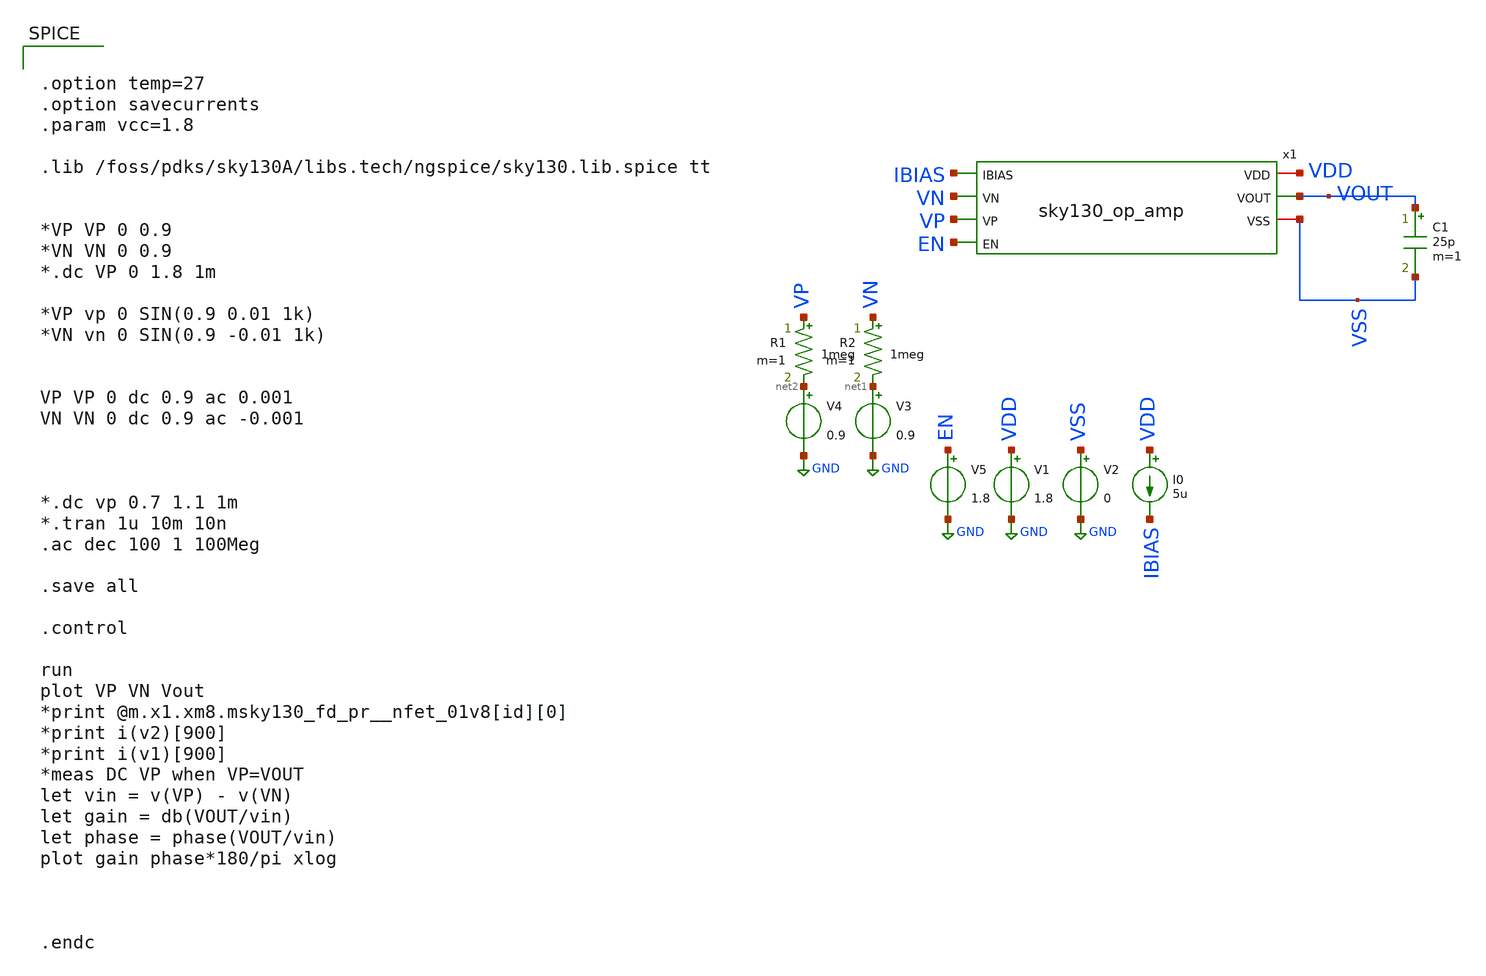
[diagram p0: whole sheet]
** sch_path: xschem/sky130_op_amp_tb.sch
**.subckt sky130_op_amp_tb
C1 VOUT VSS 25p m=1
V2 VSS GND 0
I0 VDD IBIAS 5u
V3 net1 GND 0.9
V4 net2 GND 0.9
V5 EN GND 1.8
R1 VP net2 1meg m=1
R2 VN net1 1meg m=1
V1 VDD GND 1.8
x1 VDD IBIAS VN VP VOUT EN VSS sky130_op_amp
**** begin user architecture code


.option temp=27
.option savecurrents
.param vcc=1.8

.lib /foss/pdks/sky130A/libs.tech/ngspice/sky130.lib.spice tt


*VP VP 0 0.9
*VN VN 0 0.9
*.dc VP 0 1.8 1m

*VP vp 0 SIN(0.9 0.01 1k)
*VN vn 0 SIN(0.9 -0.01 1k)


VP VP 0 dc 0.9 ac 0.001
VN VN 0 dc 0.9 ac -0.001



*.dc vp 0.7 1.1 1m
*.tran 1u 10m 10n
.ac dec 100 1 100Meg

.save all

.control

run
plot VP VN Vout
*print @m.x1.xm8.msky130_fd_pr__nfet_01v8[id][0]
*print i(v2)[900]
*print i(v1)[900]
*meas DC VP when VP=VOUT
let vin = v(VP) - v(VN)
let gain = db(VOUT/vin)
let phase = phase(VOUT/vin)
plot gain phase*180/pi xlog



.endc





**** end user architecture code
**.ends

* expanding   symbol:  sky130_op_amp.sym # of pins=7
** sym_path: xschem/sky130_op_amp.sym
** sch_path: xschem/sky130_op_amp.sch
.subckt sky130_op_amp VDD IBIAS VN VP VOUT EN VSS
*.ipin VN
*.opin VOUT
*.iopin VDD
*.iopin VSS
*.ipin VP
*.ipin EN
*.ipin IBIAS
XM1 D1 VN VTAIL VSS sky130_fd_pr__nfet_01v8 L=1 W=4 nf=4 ad='int((nf+1)/2) * W/nf * 0.29' as='int((nf+2)/2) * W/nf * 0.29'
+ pd='2*int((nf+1)/2) * (W/nf + 0.29)' ps='2*int((nf+2)/2) * (W/nf + 0.29)' nrd='0.29 / W' nrs='0.29 / W'
+ sa=0 sb=0 sd=0 mult=4 m=4
XM2 D2 VP VTAIL VSS sky130_fd_pr__nfet_01v8 L=1 W=4 nf=4 ad='int((nf+1)/2) * W/nf * 0.29' as='int((nf+2)/2) * W/nf * 0.29'
+ pd='2*int((nf+1)/2) * (W/nf + 0.29)' ps='2*int((nf+2)/2) * (W/nf + 0.29)' nrd='0.29 / W' nrs='0.29 / W'
+ sa=0 sb=0 sd=0 mult=4 m=4
XM5 VTAIL IBIAS m5m9_net VSS sky130_fd_pr__nfet_01v8 L=1 W=5 nf=4 ad='int((nf+1)/2) * W/nf * 0.29' as='int((nf+2)/2) * W/nf * 0.29'
+ pd='2*int((nf+1)/2) * (W/nf + 0.29)' ps='2*int((nf+2)/2) * (W/nf + 0.29)' nrd='0.29 / W' nrs='0.29 / W'
+ sa=0 sb=0 sd=0 mult=8 m=8
XM8 IBIAS IBIAS net1 VSS sky130_fd_pr__nfet_01v8 L=1 W=4 nf=4 ad='int((nf+1)/2) * W/nf * 0.29' as='int((nf+2)/2) * W/nf * 0.29'
+ pd='2*int((nf+1)/2) * (W/nf + 0.29)' ps='2*int((nf+2)/2) * (W/nf + 0.29)' nrd='0.29 / W' nrs='0.29 / W'
+ sa=0 sb=0 sd=0 mult=1 m=1
XM3 D1 D1 VDD VDD sky130_fd_pr__pfet_01v8 L=1 W=4 nf=4 ad='int((nf+1)/2) * W/nf * 0.29' as='int((nf+2)/2) * W/nf * 0.29'
+ pd='2*int((nf+1)/2) * (W/nf + 0.29)' ps='2*int((nf+2)/2) * (W/nf + 0.29)' nrd='0.29 / W' nrs='0.29 / W'
+ sa=0 sb=0 sd=0 mult=2 m=2
XM4 D2 D1 VDD VDD sky130_fd_pr__pfet_01v8 L=1 W=4 nf=4 ad='int((nf+1)/2) * W/nf * 0.29' as='int((nf+2)/2) * W/nf * 0.29'
+ pd='2*int((nf+1)/2) * (W/nf + 0.29)' ps='2*int((nf+2)/2) * (W/nf + 0.29)' nrd='0.29 / W' nrs='0.29 / W'
+ sa=0 sb=0 sd=0 mult=2 m=2
XM6 VOUT D2 VDD VDD sky130_fd_pr__pfet_01v8 L=1 W=4 nf=4 ad='int((nf+1)/2) * W/nf * 0.29' as='int((nf+2)/2) * W/nf * 0.29'
+ pd='2*int((nf+1)/2) * (W/nf + 0.29)' ps='2*int((nf+2)/2) * (W/nf + 0.29)' nrd='0.29 / W' nrs='0.29 / W'
+ sa=0 sb=0 sd=0 mult=7 m=7
XM7 VOUT IBIAS m7m10_net VSS sky130_fd_pr__nfet_01v8 L=1 W=5 nf=4 ad='int((nf+1)/2) * W/nf * 0.29' as='int((nf+2)/2) * W/nf * 0.29'
+ pd='2*int((nf+1)/2) * (W/nf + 0.29)' ps='2*int((nf+2)/2) * (W/nf + 0.29)' nrd='0.29 / W' nrs='0.29 / W'
+ sa=0 sb=0 sd=0 mult=12 m=12
XC1 Cin VOUT sky130_fd_pr__cap_mim_m3_1 W=75 L=35 MF=1 m=1
XM9 m5m9_net EN VSS VSS sky130_fd_pr__nfet_01v8 L=1 W=4 nf=4 ad='int((nf+1)/2) * W/nf * 0.29' as='int((nf+2)/2) * W/nf * 0.29'
+ pd='2*int((nf+1)/2) * (W/nf + 0.29)' ps='2*int((nf+2)/2) * (W/nf + 0.29)' nrd='0.29 / W' nrs='0.29 / W'
+ sa=0 sb=0 sd=0 mult=6 m=6
XM10 m7m10_net EN VSS VSS sky130_fd_pr__nfet_01v8 L=1 W=4 nf=4 ad='int((nf+1)/2) * W/nf * 0.29' as='int((nf+2)/2) * W/nf * 0.29'
+ pd='2*int((nf+1)/2) * (W/nf + 0.29)' ps='2*int((nf+2)/2) * (W/nf + 0.29)' nrd='0.29 / W' nrs='0.29 / W'
+ sa=0 sb=0 sd=0 mult=11 m=11
XM11 net1 EN VSS VSS sky130_fd_pr__nfet_01v8 L=1 W=4 nf=4 ad='int((nf+1)/2) * W/nf * 0.29' as='int((nf+2)/2) * W/nf * 0.29'
+ pd='2*int((nf+1)/2) * (W/nf + 0.29)' ps='2*int((nf+2)/2) * (W/nf + 0.29)' nrd='0.29 / W' nrs='0.29 / W'
+ sa=0 sb=0 sd=0 mult=6 m=6
XR2 Cin D2 VSS sky130_fd_pr__res_xhigh_po_1p41 L=11 mult=1 m=1
**** begin user architecture code




**** end user architecture code
XM12 VSS VSS VSS VSS sky130_fd_pr__nfet_01v8 L=1 W=1 nf=1 ad='int((nf+1)/2) * W/nf * 0.29' as='int((nf+2)/2) * W/nf * 0.29'
+ pd='2*int((nf+1)/2) * (W/nf + 0.29)' ps='2*int((nf+2)/2) * (W/nf + 0.29)' nrd='0.29 / W' nrs='0.29 / W'
+ sa=0 sb=0 sd=0 mult=4 m=4
XM13 D1 VSS VSS VSS sky130_fd_pr__nfet_01v8 L=1 W=1 nf=1 ad='int((nf+1)/2) * W/nf * 0.29' as='int((nf+2)/2) * W/nf * 0.29'
+ pd='2*int((nf+1)/2) * (W/nf + 0.29)' ps='2*int((nf+2)/2) * (W/nf + 0.29)' nrd='0.29 / W' nrs='0.29 / W'
+ sa=0 sb=0 sd=0 mult=2 m=2
XM14 D2 VSS VSS VSS sky130_fd_pr__nfet_01v8 L=1 W=1 nf=1 ad='int((nf+1)/2) * W/nf * 0.29' as='int((nf+2)/2) * W/nf * 0.29'
+ pd='2*int((nf+1)/2) * (W/nf + 0.29)' ps='2*int((nf+2)/2) * (W/nf + 0.29)' nrd='0.29 / W' nrs='0.29 / W'
+ sa=0 sb=0 sd=0 mult=2 m=2
XM15 VTAIL VSS VSS VSS sky130_fd_pr__nfet_01v8 L=1 W=1 nf=1 ad='int((nf+1)/2) * W/nf * 0.29' as='int((nf+2)/2) * W/nf * 0.29'
+ pd='2*int((nf+1)/2) * (W/nf + 0.29)' ps='2*int((nf+2)/2) * (W/nf + 0.29)' nrd='0.29 / W' nrs='0.29 / W'
+ sa=0 sb=0 sd=0 mult=8 m=8
XM16 VDD VDD VDD VDD sky130_fd_pr__pfet_01v8 L=1 W=1 nf=1 ad='int((nf+1)/2) * W/nf * 0.29' as='int((nf+2)/2) * W/nf * 0.29'
+ pd='2*int((nf+1)/2) * (W/nf + 0.29)' ps='2*int((nf+2)/2) * (W/nf + 0.29)' nrd='0.29 / W' nrs='0.29 / W'
+ sa=0 sb=0 sd=0 mult=8 m=8
XM17 m5m9_net VSS VSS VSS sky130_fd_pr__nfet_01v8 L=1 W=1 nf=1 ad='int((nf+1)/2) * W/nf * 0.29' as='int((nf+2)/2) * W/nf * 0.29'
+ pd='2*int((nf+1)/2) * (W/nf + 0.29)' ps='2*int((nf+2)/2) * (W/nf + 0.29)' nrd='0.29 / W' nrs='0.29 / W'
+ sa=0 sb=0 sd=0 mult=16 m=16
XM20 VSS VSS VSS VSS sky130_fd_pr__nfet_01v8 L=1 W=1 nf=1 ad='int((nf+1)/2) * W/nf * 0.29' as='int((nf+2)/2) * W/nf * 0.29'
+ pd='2*int((nf+1)/2) * (W/nf + 0.29)' ps='2*int((nf+2)/2) * (W/nf + 0.29)' nrd='0.29 / W' nrs='0.29 / W'
+ sa=0 sb=0 sd=0 mult=12 m=12
XM21 IBIAS VSS VSS VSS sky130_fd_pr__nfet_01v8 L=1 W=1 nf=1 ad='int((nf+1)/2) * W/nf * 0.29' as='int((nf+2)/2) * W/nf * 0.29'
+ pd='2*int((nf+1)/2) * (W/nf + 0.29)' ps='2*int((nf+2)/2) * (W/nf + 0.29)' nrd='0.29 / W' nrs='0.29 / W'
+ sa=0 sb=0 sd=0 mult=2 m=2
XM22 VSS VSS VSS VSS sky130_fd_pr__nfet_01v8 L=1 W=1 nf=1 ad='int((nf+1)/2) * W/nf * 0.29' as='int((nf+2)/2) * W/nf * 0.29'
+ pd='2*int((nf+1)/2) * (W/nf + 0.29)' ps='2*int((nf+2)/2) * (W/nf + 0.29)' nrd='0.29 / W' nrs='0.29 / W'
+ sa=0 sb=0 sd=0 mult=16 m=16
XM23 m7m10_net VSS VSS VSS sky130_fd_pr__nfet_01v8 L=1 W=1 nf=1 ad='int((nf+1)/2) * W/nf * 0.29' as='int((nf+2)/2) * W/nf * 0.29'
+ pd='2*int((nf+1)/2) * (W/nf + 0.29)' ps='2*int((nf+2)/2) * (W/nf + 0.29)' nrd='0.29 / W' nrs='0.29 / W'
+ sa=0 sb=0 sd=0 mult=20 m=20
XM18 VDD VDD VDD VDD sky130_fd_pr__pfet_01v8 L=1 W=1 nf=1 ad='int((nf+1)/2) * W/nf * 0.29' as='int((nf+2)/2) * W/nf * 0.29'
+ pd='2*int((nf+1)/2) * (W/nf + 0.29)' ps='2*int((nf+2)/2) * (W/nf + 0.29)' nrd='0.29 / W' nrs='0.29 / W'
+ sa=0 sb=0 sd=0 mult=14 m=14
.ends

.GLOBAL GND
.end
